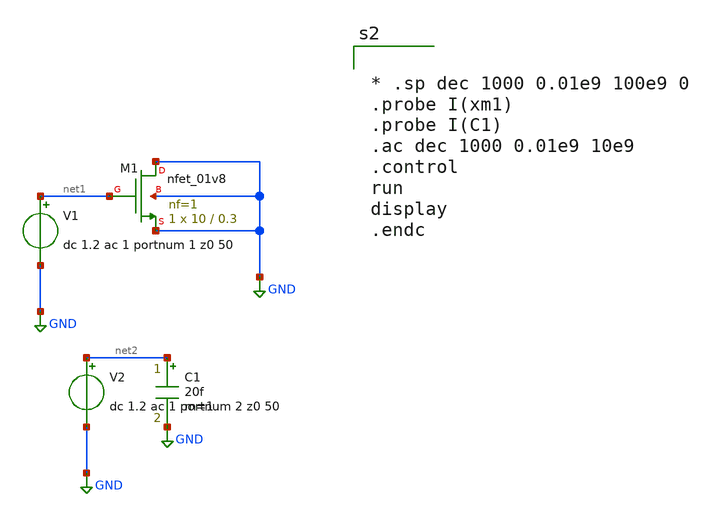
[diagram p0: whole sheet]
** sch_path: xschem/untitled-3.sch
**.subckt untitled-3
XM1 GND net1 GND GND sky130_fd_pr__nfet_01v8 L=0.3 W=10 nf=1 ad='int((nf+1)/2) * W/nf * 0.29' as='int((nf+2)/2) * W/nf * 0.29'
+ pd='2*int((nf+1)/2) * (W/nf + 0.29)' ps='2*int((nf+2)/2) * (W/nf + 0.29)' nrd='0.29 / W' nrs='0.29 / W'
+ sa=0 sb=0 sd=0 mult=1 m=1
V1 net1 GND dc 1.2 ac 1 portnum 1 z0 50
C1 net2 GND 20f m=1
V2 net2 GND dc 1.2 ac 1 portnum 2 z0 50
**** begin user architecture code
.lib $::SKYWATER_MODELS/sky130.lib.spice tt
* .include $::PDKPATH/libs.ref/sky130_fd_sc_hvl/spice/sky130_fd_sc_hvl.spice



* .sp dec 1000 0.01e9 100e9 0
.probe I(xm1)
.probe I(C1)
.ac dec 1000 0.01e9 10e9
.control
run
display
.endc


**** end user architecture code
**.ends
.GLOBAL GND
.end
